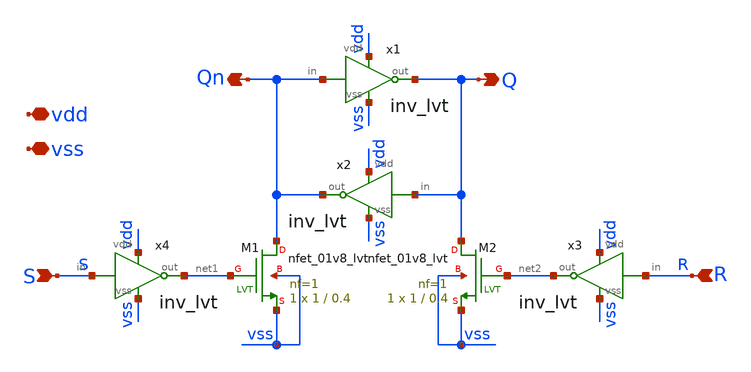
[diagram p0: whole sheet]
** sch_path: xschem/adc/latch.sch
**.subckt latch S R vss vdd Q Qn
*.ipin S
*.ipin R
*.iopin vss
*.iopin vdd
*.opin Q
*.opin Qn
x1 vdd Qn Q vss inv_lvt
x2 vdd Q Qn vss inv_lvt
x3 vdd R net2 vss inv_lvt
x4 vdd S net1 vss inv_lvt
XM1 Qn net1 vss vss sky130_fd_pr__nfet_01v8_lvt L=0.4 W=1 nf=1 ad='int((nf+1)/2) * W/nf * 0.29' as='int((nf+2)/2) * W/nf * 0.29'
+ pd='2*int((nf+1)/2) * (W/nf + 0.29)' ps='2*int((nf+2)/2) * (W/nf + 0.29)' nrd='0.29 / W' nrs='0.29 / W'
+ sa=0 sb=0 sd=0 mult=1 m=1
XM2 Q net2 vss vss sky130_fd_pr__nfet_01v8_lvt L=0.4 W=1 nf=1 ad='int((nf+1)/2) * W/nf * 0.29' as='int((nf+2)/2) * W/nf * 0.29'
+ pd='2*int((nf+1)/2) * (W/nf + 0.29)' ps='2*int((nf+2)/2) * (W/nf + 0.29)' nrd='0.29 / W' nrs='0.29 / W'
+ sa=0 sb=0 sd=0 mult=1 m=1
**.ends
.end
